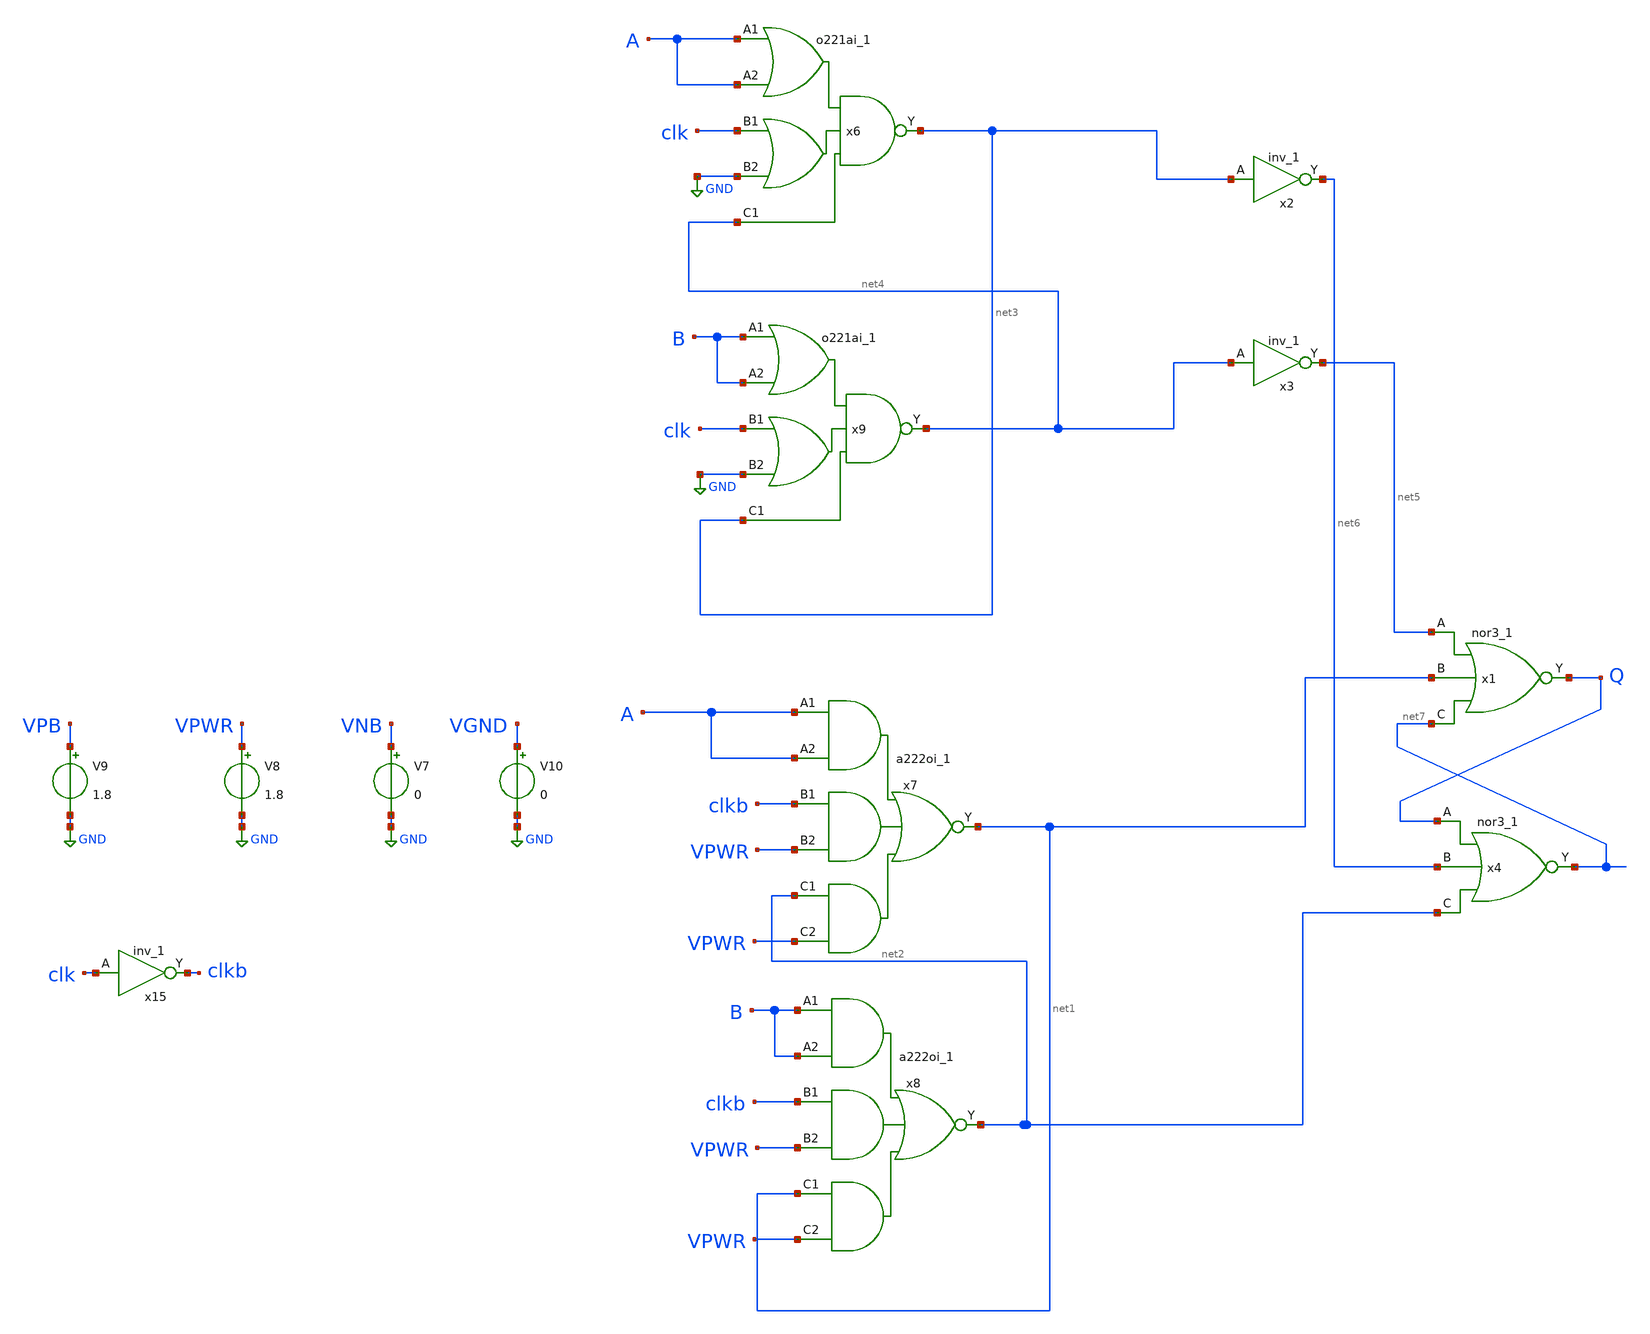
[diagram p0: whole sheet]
** sch_path: Schemtics/ADC/cmp/cmpoai_all.sch
**.subckt cmpoai_all
V7 VNB GND 0
V8 VPWR GND 1.8
V9 VPB GND 1.8
V10 VGND GND 0
x15 clk VGND VNB VPB VPWR clkb sky130_fd_sc_hd__inv_1
x7 A A clkb VPWR net2 VPWR VGND VNB VPB VPWR net1 sky130_fd_sc_hd__a222oi_1
x8 B B clkb VPWR net1 VPWR VGND VNB VPB VPWR net2 sky130_fd_sc_hd__a222oi_1
x2 net3 VGND VNB VPB VPWR net6 sky130_fd_sc_hd__inv_1
x3 net4 VGND VNB VPB VPWR net5 sky130_fd_sc_hd__inv_1
x6 A A clk GND net4 VGND VNB VPB VPWR net3 sky130_fd_sc_hd__o221ai_1
x9 B B clk GND net3 VGND VNB VPB VPWR net4 sky130_fd_sc_hd__o221ai_1
x1 net5 net1 net7 VGND VNB VPB VPWR Q sky130_fd_sc_hd__nor3_1
x4 Q net6 net2 VGND VNB VPB VPWR net7 sky130_fd_sc_hd__nor3_1
**.ends
.GLOBAL GND
.end
